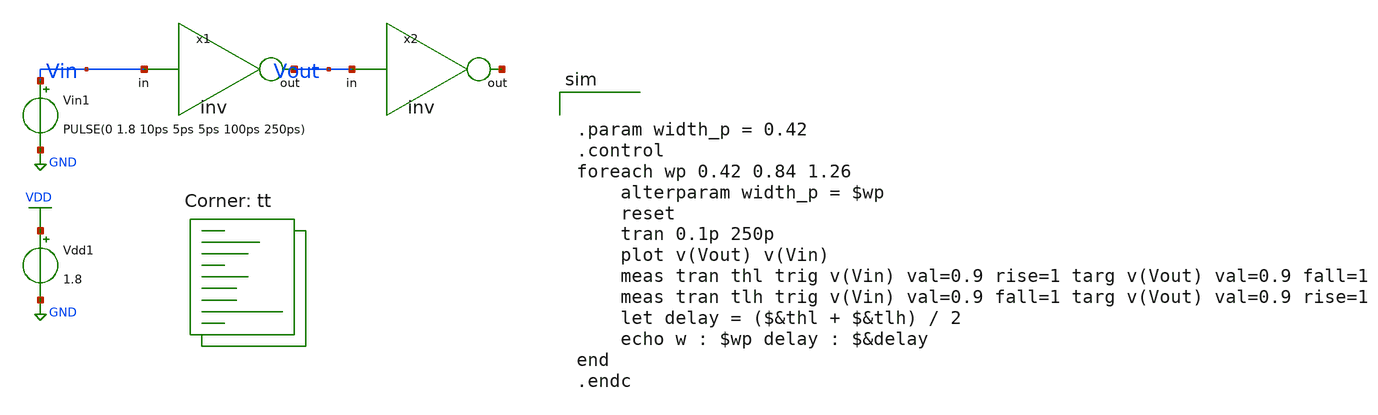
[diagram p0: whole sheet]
** sch_path: tutorial_4/tutorial_4_1a.sch
**.subckt tutorial_4_1a
x1 Vout Vin inv
x2 net1 Vout inv
Vin1 Vin GND PULSE(0 1.8 10ps 5ps 5ps 100ps 250ps)
Vdd1 VDD GND 1.8
**** begin user architecture code
.lib $::SKYWATER_MODELS/sky130.lib.spice tt


.param width_p = 0.42
.control
foreach wp 0.42 0.84 1.26
    alterparam width_p = $wp
    reset
    tran 0.1p 250p
    plot v(Vout) v(Vin)
    meas tran thl trig v(Vin) val=0.9 rise=1 targ v(Vout) val=0.9 fall=1
    meas tran tlh trig v(Vin) val=0.9 fall=1 targ v(Vout) val=0.9 rise=1
    let delay = ($&thl + $&tlh) / 2
    echo w : $wp delay : $&delay
end
.endc

**** end user architecture code
**.ends

* expanding   symbol:  /home/EE23B038/ee5311/tutorial_4/inv.sym # of pins=2
** sym_path: tutorial_4/inv.sym
** sch_path: tutorial_4/inv.sch
.subckt inv out in
*.ipin in
*.opin out
XM1 out in GND GND sky130_fd_pr__nfet_01v8 L=0.15 W=0.42 nf=1 ad='int((nf+1)/2) * W/nf * 0.29' as='int((nf+2)/2) * W/nf * 0.29'
+ pd='2*int((nf+1)/2) * (W/nf + 0.29)' ps='2*int((nf+2)/2) * (W/nf + 0.29)' nrd='0.29 / W' nrs='0.29 / W'
+ sa=0 sb=0 sd=0 mult=1 m=1
XM2 out in VDD VDD sky130_fd_pr__pfet_01v8 L=0.15 W={width_p} nf=1 ad='int((nf+1)/2) * W/nf * 0.29' as='int((nf+2)/2) * W/nf * 0.29'
+ pd='2*int((nf+1)/2) * (W/nf + 0.29)' ps='2*int((nf+2)/2) * (W/nf + 0.29)' nrd='0.29 / W' nrs='0.29 / W'
+ sa=0 sb=0 sd=0 mult=1 m=1
.ends

.GLOBAL GND
.GLOBAL VDD
.end
